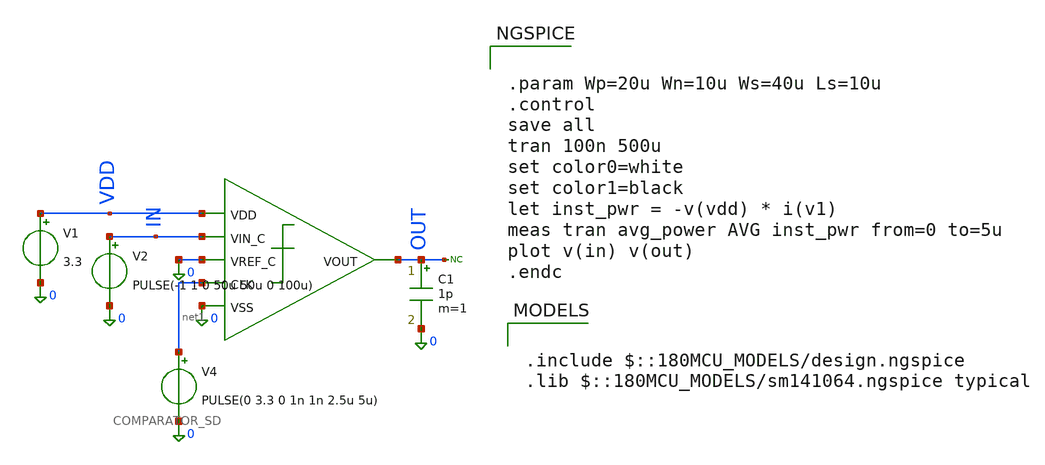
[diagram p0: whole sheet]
** sch_path: src/schematics/latched comparator/COMP_TB.sch
**.subckt COMP_TB
* noconn OUT
V2 IN 0 PULSE(-1 1 0 50u 50u 0 100u)
V4 net1 0 PULSE(0 3.3 0 1n 1n 2.5u 5u)
V1 VDD 0 3.3
x1 VDD IN 0 net1 OUT 0 COMPARATOR_SD
C1 OUT 0 1p m=1
**** begin user architecture code


.param Wp=20u Wn=10u Ws=40u Ls=10u
.control
save all
tran 100n 500u
set color0=white
set color1=black
let inst_pwr = -v(vdd) * i(v1)
meas tran avg_power AVG inst_pwr from=0 to=5u
plot v(in) v(out)
.endc




.include $::180MCU_MODELS/design.ngspice
.lib $::180MCU_MODELS/sm141064.ngspice typical

**** end user architecture code
**.ends
.end
